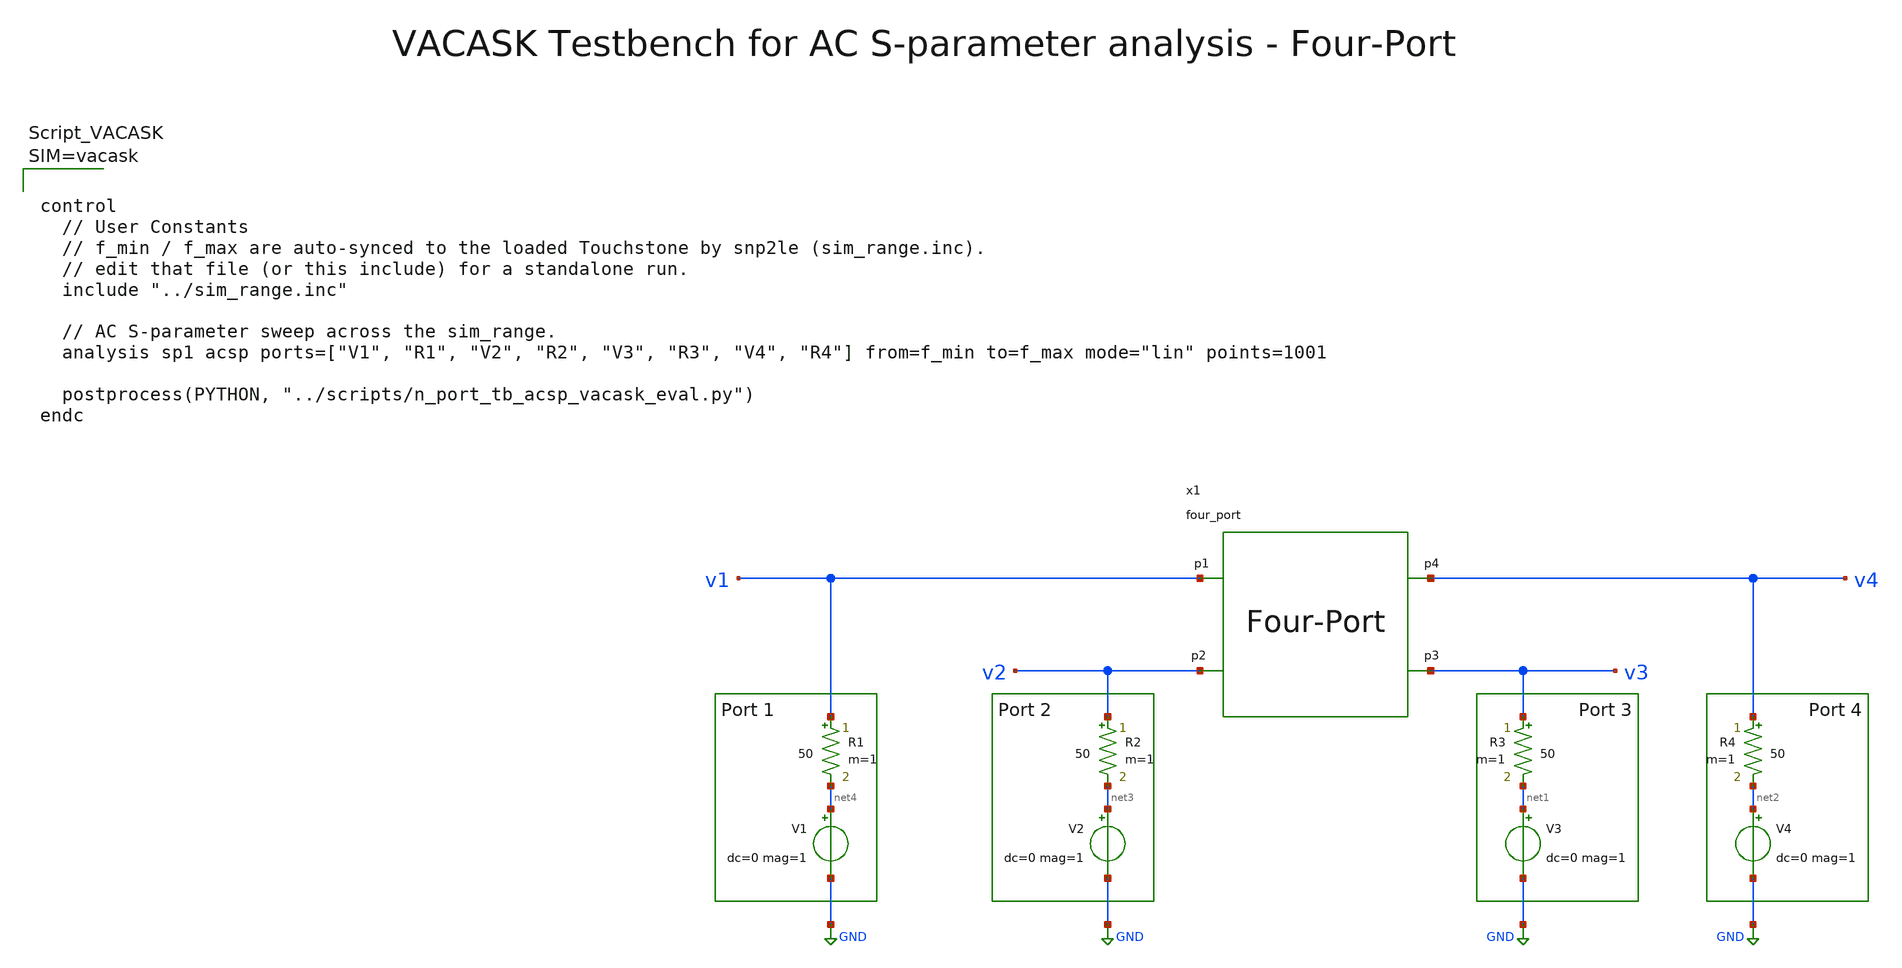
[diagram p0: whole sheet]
** sch_path: testbenches/xschem/four_port_tb_acsp_vacask.sch
**.subckt four_port_tb_acsp_vacask
x1 v1 v2 v3 v4 four_port
R3 v3 net1 50 m=1
V3 net1 GND dc=0 mag=1
R4 v4 net2 50 m=1
V4 net2 GND dc=0 mag=1
R1 v1 net4 50 m=1
V1 net4 GND dc=0 mag=1
R2 v2 net3 50 m=1
V2 net3 GND dc=0 mag=1
**** begin user architecture code






**** end user architecture code
**.ends
.GLOBAL GND
.end
